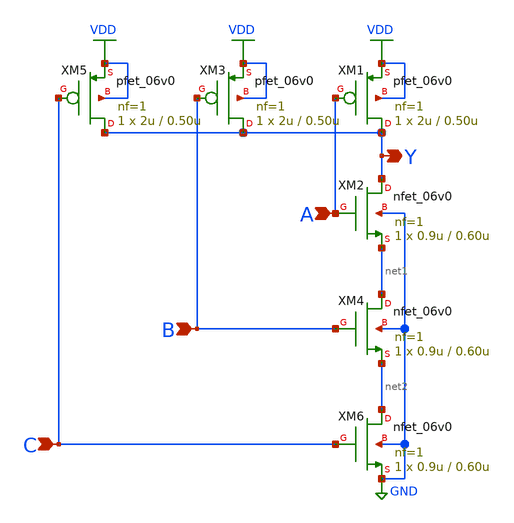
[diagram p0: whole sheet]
** sch_path: nand3.sch
**.subckt nand3 B A Y C
*.ipin B
*.ipin A
*.opin Y
*.ipin C
XM3 Y B VDD VDD pfet_06v0 L=0.50u W=2u nf=1 ad='int((nf+1)/2) * W/nf * 0.18u' as='int((nf+2)/2) * W/nf * 0.18u'
+ pd='2*int((nf+1)/2) * (W/nf + 0.18u)' ps='2*int((nf+2)/2) * (W/nf + 0.18u)' nrd='0.18u / W' nrs='0.18u / W'
+ sa=0 sb=0 sd=0 m=1
XM1 Y A VDD VDD pfet_06v0 L=0.50u W=2u nf=1 ad='int((nf+1)/2) * W/nf * 0.18u' as='int((nf+2)/2) * W/nf * 0.18u'
+ pd='2*int((nf+1)/2) * (W/nf + 0.18u)' ps='2*int((nf+2)/2) * (W/nf + 0.18u)' nrd='0.18u / W' nrs='0.18u / W'
+ sa=0 sb=0 sd=0 m=1
XM2 Y A net1 GND nfet_06v0 L=0.60u W=0.9u nf=1 ad='int((nf+1)/2) * W/nf * 0.18u' as='int((nf+2)/2) * W/nf * 0.18u'
+ pd='2*int((nf+1)/2) * (W/nf + 0.18u)' ps='2*int((nf+2)/2) * (W/nf + 0.18u)' nrd='0.18u / W' nrs='0.18u / W'
+ sa=0 sb=0 sd=0 m=1
XM4 net1 B net2 GND nfet_06v0 L=0.60u W=0.9u nf=1 ad='int((nf+1)/2) * W/nf * 0.18u' as='int((nf+2)/2) * W/nf * 0.18u'
+ pd='2*int((nf+1)/2) * (W/nf + 0.18u)' ps='2*int((nf+2)/2) * (W/nf + 0.18u)' nrd='0.18u / W' nrs='0.18u / W'
+ sa=0 sb=0 sd=0 m=1
XM5 Y C VDD VDD pfet_06v0 L=0.50u W=2u nf=1 ad='int((nf+1)/2) * W/nf * 0.18u' as='int((nf+2)/2) * W/nf * 0.18u'
+ pd='2*int((nf+1)/2) * (W/nf + 0.18u)' ps='2*int((nf+2)/2) * (W/nf + 0.18u)' nrd='0.18u / W' nrs='0.18u / W'
+ sa=0 sb=0 sd=0 m=1
XM6 net2 C GND GND nfet_06v0 L=0.60u W=0.9u nf=1 ad='int((nf+1)/2) * W/nf * 0.18u' as='int((nf+2)/2) * W/nf * 0.18u'
+ pd='2*int((nf+1)/2) * (W/nf + 0.18u)' ps='2*int((nf+2)/2) * (W/nf + 0.18u)' nrd='0.18u / W' nrs='0.18u / W'
+ sa=0 sb=0 sd=0 m=1
**.ends
.GLOBAL VDD
.GLOBAL GND
.end
